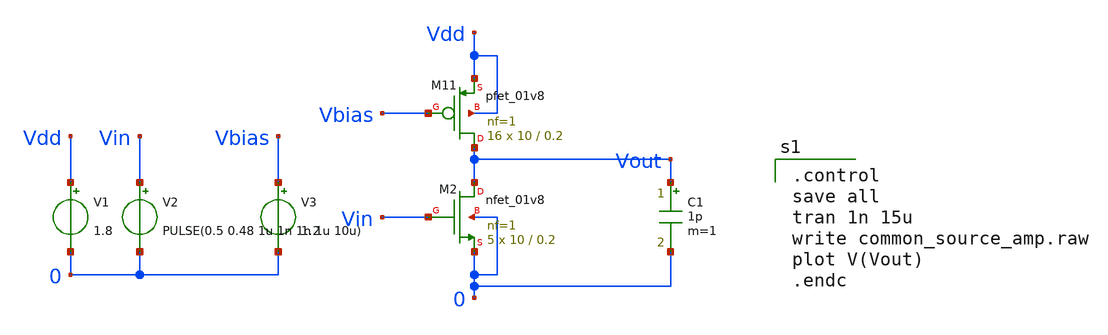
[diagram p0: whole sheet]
** sch_path: common_source_amp.sch
**.subckt common_source_amp
XM2 Vout Vin 0 0 sky130_fd_pr__nfet_01v8 L=0.2 W=10 nf=1 ad='int((1 + 1)/2) * 10 / 1 * 0.29' as='int((1 + 2)/2) * 10 / 1 * 0.29'
+ pd='2*int((1 + 1)/2) * (10 / 1 + 0.29)' ps='2*int((1 + 2)/2) * (10 / 1 + 0.29)' nrd='0.29 / 10 ' nrs='0.29 / 10 '
+ sa=0 sb=0 sd=0 mult=5 m=5
XM11 Vout Vbias Vdd Vdd sky130_fd_pr__pfet_01v8 L=0.2 W=10 nf=1 ad='int((nf+1)/2) * W/nf * 0.29' as='int((nf+2)/2) * W/nf * 0.29'
+ pd='2*int((nf+1)/2) * (W/nf + 0.29)' ps='2*int((nf+2)/2) * (W/nf + 0.29)' nrd='0.29 / W' nrs='0.29 / W'
+ sa=0 sb=0 sd=0 mult=16 m=16
C1 Vout 0 1p m=1
V1 Vdd 0 1.8
V2 Vin 0 PULSE(0.5 0.48 1u 1n 1n 1u 10u)
V3 Vbias 0 1.2
**** begin user architecture code

** opencircuitdesign pdks install
.lib $::SKYWATER_MODELS/sky130.lib.spice tt



.control
save all
tran 1n 15u
write common_source_amp.raw
plot V(Vout)
.endc

**** end user architecture code
**.ends
.end
